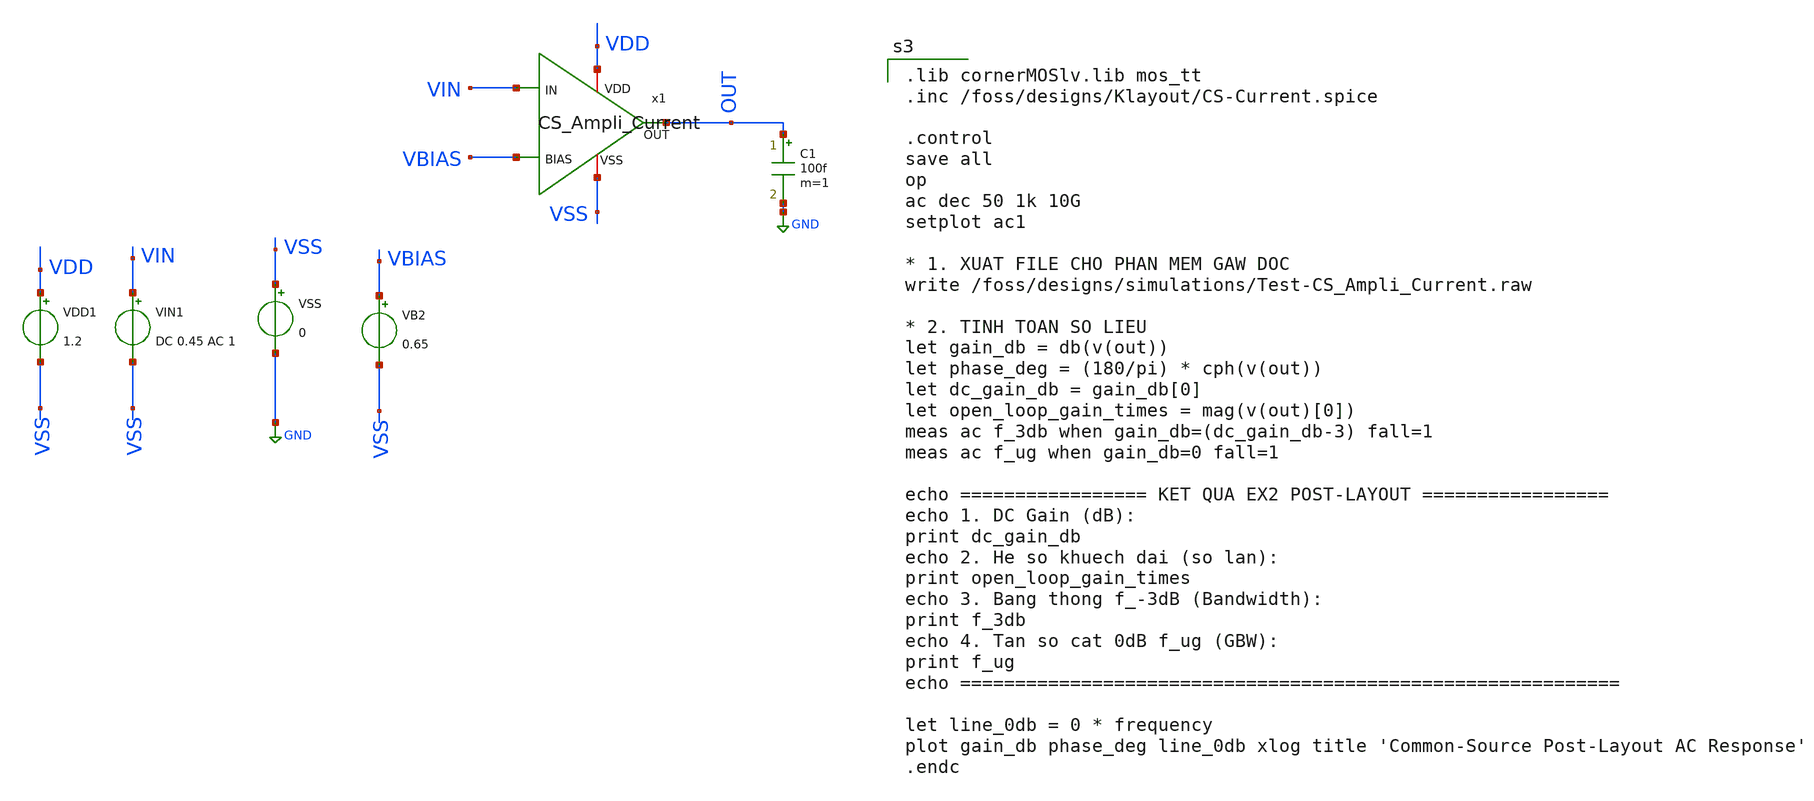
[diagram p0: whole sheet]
** sch_path: BTDay6-Ex/TestGaw-CS_Ampli_Current.sch
**.subckt TestGaw-CS_Ampli_Current
C1 OUT GND 100f m=1
x1 VBIAS VIN VDD OUT VSS CS_Ampli_Current
VDD1 VDD VSS 1.2
VSS VSS GND 0
VB2 VBIAS VSS 0.65
VIN1 VIN VSS DC 0.45 AC 1
**** begin user architecture code

.lib cornerMOSlv.lib mos_tt
.inc /foss/designs/Klayout/CS-Current.spice

.control
save all
op
ac dec 50 1k 10G
setplot ac1

* 1. XUAT FILE CHO PHAN MEM GAW DOC
write /foss/designs/simulations/Test-CS_Ampli_Current.raw

* 2. TINH TOAN SO LIEU
let gain_db = db(v(out))
let phase_deg = (180/pi) * cph(v(out))
let dc_gain_db = gain_db[0]
let open_loop_gain_times = mag(v(out)[0])
meas ac f_3db when gain_db=(dc_gain_db-3) fall=1
meas ac f_ug when gain_db=0 fall=1

echo ================= KET QUA EX2 POST-LAYOUT =================
echo 1. DC Gain (dB):
print dc_gain_db
echo 2. He so khuech dai (so lan):
print open_loop_gain_times
echo 3. Bang thong f_-3dB (Bandwidth):
print f_3db
echo 4. Tan so cat 0dB f_ug (GBW):
print f_ug
echo ============================================================

let line_0db = 0 * frequency
plot gain_db phase_deg line_0db xlog title 'Common-Source Post-Layout AC Response'
.endc


**** end user architecture code
**.ends
.GLOBAL GND
.end
